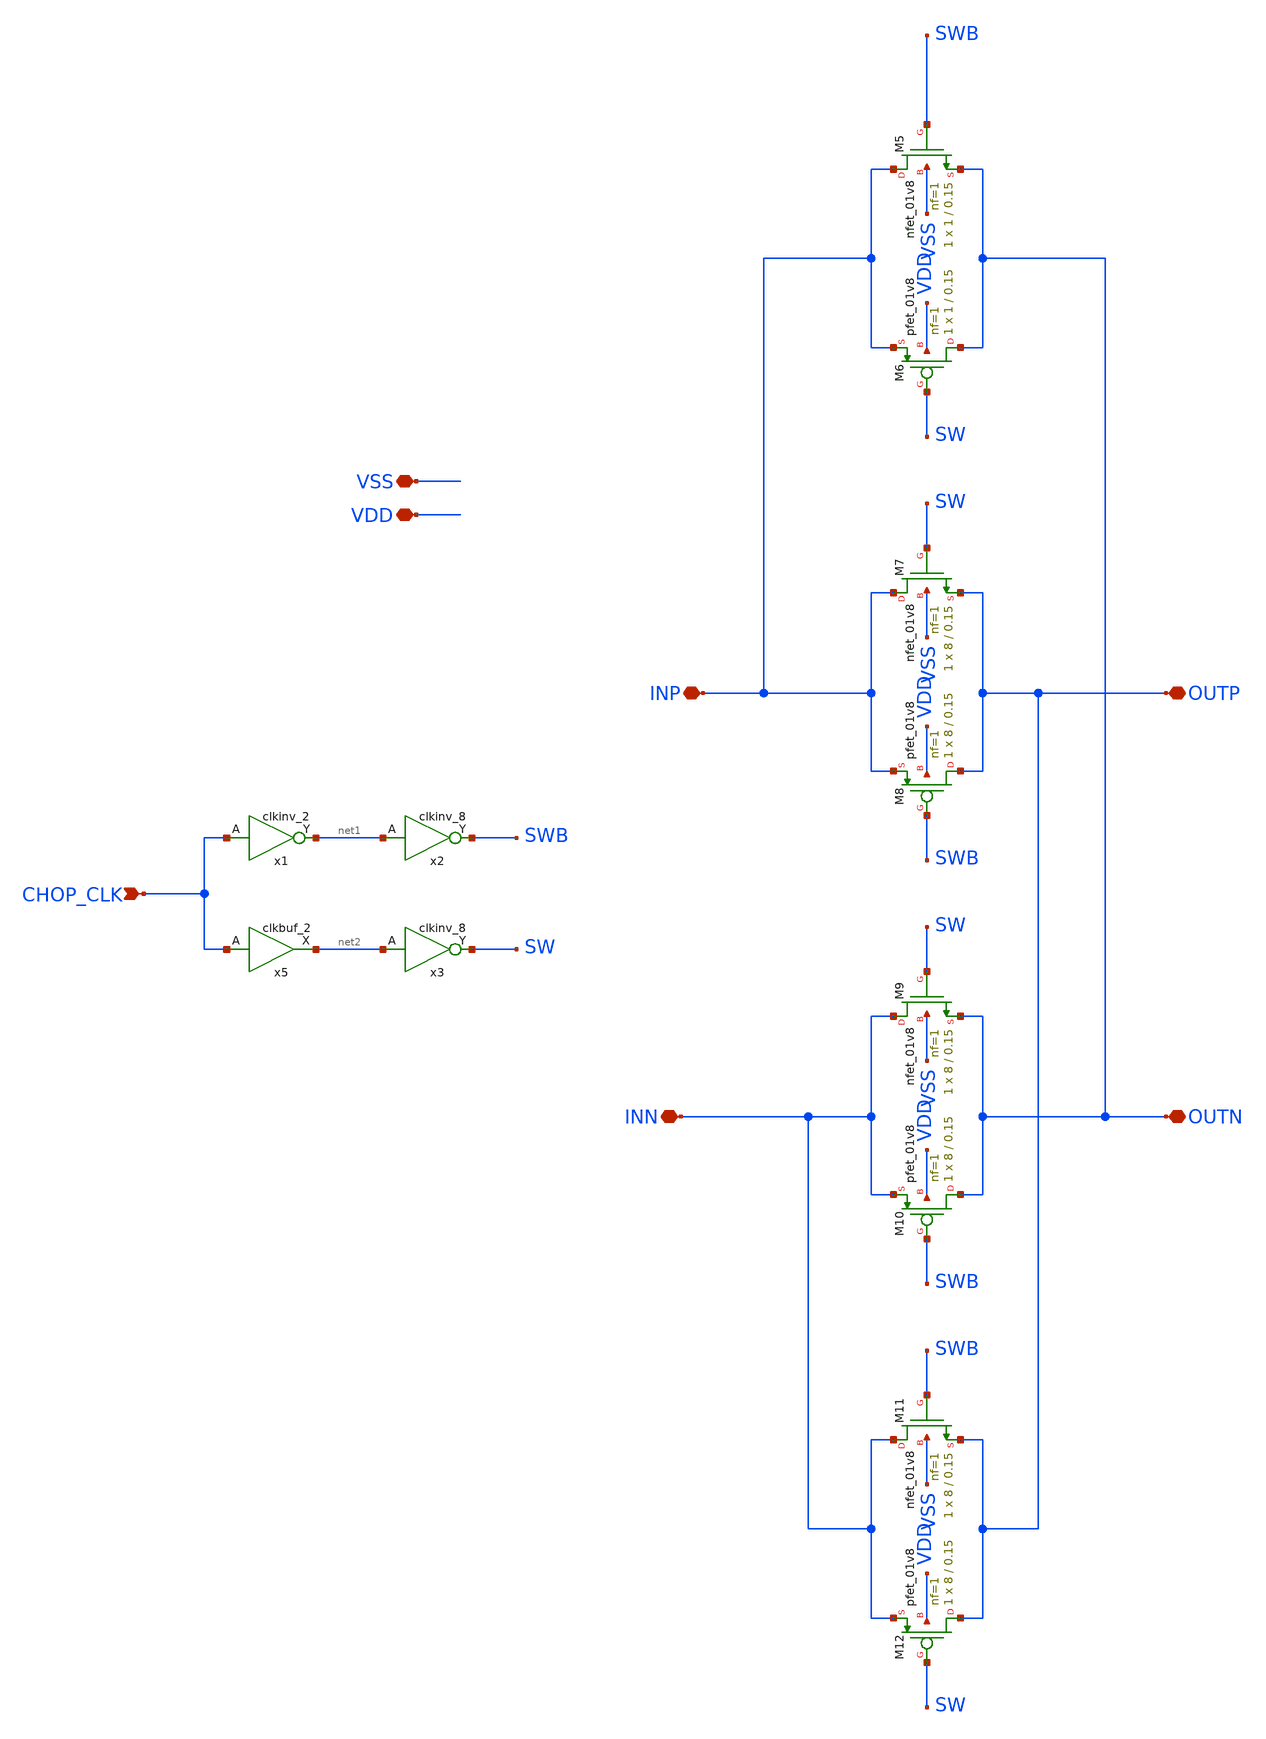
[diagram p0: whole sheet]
** sch_path: opamp_lna/chopper.sch
**.subckt chopper CHOP_CLK INP INN OUTP OUTN VSS VDD
*.ipin CHOP_CLK
*.iopin INP
*.iopin INN
*.iopin OUTP
*.iopin OUTN
*.iopin VSS
*.iopin VDD
x5 CHOP_CLK VSS VNB VPB VDD net2 sky130_fd_sc_hd__clkbuf_2
x1 CHOP_CLK VGND VNB VPB VPWR net1 sky130_fd_sc_hd__clkinv_2
x2 net1 VSS VNB VPB VDD SWB sky130_fd_sc_hd__clkinv_8
x3 net2 VSS VNB VPB VDD SW sky130_fd_sc_hd__clkinv_8
XM5 INP SWB OUTN VSS sky130_fd_pr__nfet_01v8 L=0.15 W=1 nf=1 ad='int((nf+1)/2) * W/nf * 0.29' as='int((nf+2)/2) * W/nf * 0.29'
+ pd='2*int((nf+1)/2) * (W/nf + 0.29)' ps='2*int((nf+2)/2) * (W/nf + 0.29)' nrd='0.29 / W' nrs='0.29 / W'
+ sa=0 sb=0 sd=0 mult=1 m=1
XM6 OUTN SW INP VDD sky130_fd_pr__pfet_01v8 L=0.15 W=1 nf=1 ad='int((nf+1)/2) * W/nf * 0.29' as='int((nf+2)/2) * W/nf * 0.29'
+ pd='2*int((nf+1)/2) * (W/nf + 0.29)' ps='2*int((nf+2)/2) * (W/nf + 0.29)' nrd='0.29 / W' nrs='0.29 / W'
+ sa=0 sb=0 sd=0 mult=1 m=1
XM7 INP SW OUTP VSS sky130_fd_pr__nfet_01v8 L=0.15 W=8 nf=1 ad='int((nf+1)/2) * W/nf * 0.29' as='int((nf+2)/2) * W/nf * 0.29'
+ pd='2*int((nf+1)/2) * (W/nf + 0.29)' ps='2*int((nf+2)/2) * (W/nf + 0.29)' nrd='0.29 / W' nrs='0.29 / W'
+ sa=0 sb=0 sd=0 mult=1 m=1
XM8 OUTP SWB INP VDD sky130_fd_pr__pfet_01v8 L=0.15 W=8 nf=1 ad='int((nf+1)/2) * W/nf * 0.29' as='int((nf+2)/2) * W/nf * 0.29'
+ pd='2*int((nf+1)/2) * (W/nf + 0.29)' ps='2*int((nf+2)/2) * (W/nf + 0.29)' nrd='0.29 / W' nrs='0.29 / W'
+ sa=0 sb=0 sd=0 mult=1 m=1
XM9 INN SW OUTN VSS sky130_fd_pr__nfet_01v8 L=0.15 W=8 nf=1 ad='int((nf+1)/2) * W/nf * 0.29' as='int((nf+2)/2) * W/nf * 0.29'
+ pd='2*int((nf+1)/2) * (W/nf + 0.29)' ps='2*int((nf+2)/2) * (W/nf + 0.29)' nrd='0.29 / W' nrs='0.29 / W'
+ sa=0 sb=0 sd=0 mult=1 m=1
XM10 OUTN SWB INN VDD sky130_fd_pr__pfet_01v8 L=0.15 W=8 nf=1 ad='int((nf+1)/2) * W/nf * 0.29' as='int((nf+2)/2) * W/nf * 0.29'
+ pd='2*int((nf+1)/2) * (W/nf + 0.29)' ps='2*int((nf+2)/2) * (W/nf + 0.29)' nrd='0.29 / W' nrs='0.29 / W'
+ sa=0 sb=0 sd=0 mult=1 m=1
XM11 INN SWB OUTP VSS sky130_fd_pr__nfet_01v8 L=0.15 W=8 nf=1 ad='int((nf+1)/2) * W/nf * 0.29' as='int((nf+2)/2) * W/nf * 0.29'
+ pd='2*int((nf+1)/2) * (W/nf + 0.29)' ps='2*int((nf+2)/2) * (W/nf + 0.29)' nrd='0.29 / W' nrs='0.29 / W'
+ sa=0 sb=0 sd=0 mult=1 m=1
XM12 OUTP SW INN VDD sky130_fd_pr__pfet_01v8 L=0.15 W=8 nf=1 ad='int((nf+1)/2) * W/nf * 0.29' as='int((nf+2)/2) * W/nf * 0.29'
+ pd='2*int((nf+1)/2) * (W/nf + 0.29)' ps='2*int((nf+2)/2) * (W/nf + 0.29)' nrd='0.29 / W' nrs='0.29 / W'
+ sa=0 sb=0 sd=0 mult=1 m=1
**.ends
.end
